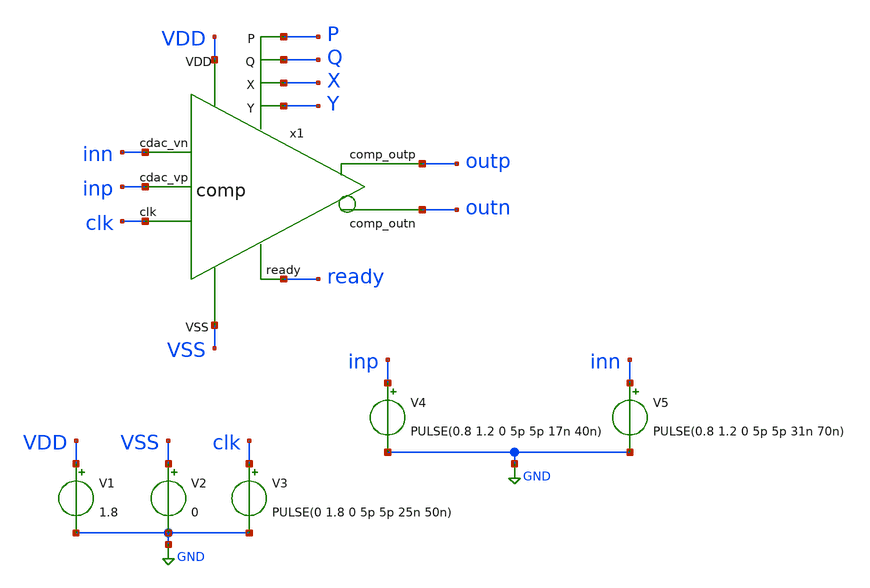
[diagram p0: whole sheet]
** sch_path: module/comparator/tb_comp.sch
**.subckt tb_comp
x1 X Y ready outn outp inn inp clk VDD VSS Q P comp
V1 VDD GND 1.8
V2 VSS GND 0
V3 clk GND PULSE(0 1.8 0 5p 5p 25n 50n)
V4 inp GND PULSE(0.8 1.2 0 5p 5p 17n 40n)
V5 inn GND PULSE(0.8 1.2 0 5p 5p 31n 70n)
**** begin user architecture code



.lib /foss/pdks/sky130A/libs.tech/ngspice/sky130.lib.spice tt

.tran 49ns 51ns
.control
    run
    plot V(outp)+8 V(P)-2  V(X)+4  V(clk) V(inn) V(inp) V(Y)+2  V(outn)+6 V(Q)-2 V(ready)+10
.endc
.save all



**** end user architecture code
**.ends

* expanding   symbol:  /foss/designs/goss_test/module/comparator/comp.sym # of pins=12
** sym_path: module/comparator/comp.sym
** sch_path: module/comparator/comp.sch
.subckt comp X Y ready comp_outn comp_outp cdac_vn cdac_vp clk VDD VSS Q P
*.ipin cdac_vn
*.ipin cdac_vp
*.ipin VSS
*.ipin VDD
*.opin comp_outp
*.opin comp_outn
*.opin ready
*.ipin clk
*.opin X
*.opin Y
*.opin P
*.opin Q
XM1 net1 clk VSS VSS sky130_fd_pr__nfet_01v8 L=0.15 W=4 nf=1 ad='int((nf+1)/2) * W/nf * 0.29' as='int((nf+2)/2) * W/nf * 0.29'
+ pd='2*int((nf+1)/2) * (W/nf + 0.29)' ps='2*int((nf+2)/2) * (W/nf + 0.29)' nrd='0.29 / W' nrs='0.29 / W'
+ sa=0 sb=0 sd=0 mult=1 m=1
XM2 P cdac_vp net1 VSS sky130_fd_pr__nfet_01v8 L=0.15 W=4 nf=1 ad='int((nf+1)/2) * W/nf * 0.29' as='int((nf+2)/2) * W/nf * 0.29'
+ pd='2*int((nf+1)/2) * (W/nf + 0.29)' ps='2*int((nf+2)/2) * (W/nf + 0.29)' nrd='0.29 / W' nrs='0.29 / W'
+ sa=0 sb=0 sd=0 mult=1 m=1
XM3 Q cdac_vn net1 VSS sky130_fd_pr__nfet_01v8 L=0.15 W=4 nf=1 ad='int((nf+1)/2) * W/nf * 0.29' as='int((nf+2)/2) * W/nf * 0.29'
+ pd='2*int((nf+1)/2) * (W/nf + 0.29)' ps='2*int((nf+2)/2) * (W/nf + 0.29)' nrd='0.29 / W' nrs='0.29 / W'
+ sa=0 sb=0 sd=0 mult=1 m=1
XM4 Y X Q VSS sky130_fd_pr__nfet_01v8 L=0.15 W=8 nf=1 ad='int((nf+1)/2) * W/nf * 0.29' as='int((nf+2)/2) * W/nf * 0.29'
+ pd='2*int((nf+1)/2) * (W/nf + 0.29)' ps='2*int((nf+2)/2) * (W/nf + 0.29)' nrd='0.29 / W' nrs='0.29 / W'
+ sa=0 sb=0 sd=0 mult=1 m=1
XM5 X Y P VSS sky130_fd_pr__nfet_01v8 L=0.15 W=8 nf=1 ad='int((nf+1)/2) * W/nf * 0.29' as='int((nf+2)/2) * W/nf * 0.29'
+ pd='2*int((nf+1)/2) * (W/nf + 0.29)' ps='2*int((nf+2)/2) * (W/nf + 0.29)' nrd='0.29 / W' nrs='0.29 / W'
+ sa=0 sb=0 sd=0 mult=1 m=1
XM6 X Y VDD VDD sky130_fd_pr__pfet_01v8 L=0.15 W=2 nf=1 ad='int((nf+1)/2) * W/nf * 0.29' as='int((nf+2)/2) * W/nf * 0.29'
+ pd='2*int((nf+1)/2) * (W/nf + 0.29)' ps='2*int((nf+2)/2) * (W/nf + 0.29)' nrd='0.29 / W' nrs='0.29 / W'
+ sa=0 sb=0 sd=0 mult=1 m=1
XM7 Y X VDD VDD sky130_fd_pr__pfet_01v8 L=0.15 W=2 nf=1 ad='int((nf+1)/2) * W/nf * 0.29' as='int((nf+2)/2) * W/nf * 0.29'
+ pd='2*int((nf+1)/2) * (W/nf + 0.29)' ps='2*int((nf+2)/2) * (W/nf + 0.29)' nrd='0.29 / W' nrs='0.29 / W'
+ sa=0 sb=0 sd=0 mult=1 m=1
XM8 X clk VDD VDD sky130_fd_pr__pfet_01v8 L=0.15 W=2 nf=1 ad='int((nf+1)/2) * W/nf * 0.29' as='int((nf+2)/2) * W/nf * 0.29'
+ pd='2*int((nf+1)/2) * (W/nf + 0.29)' ps='2*int((nf+2)/2) * (W/nf + 0.29)' nrd='0.29 / W' nrs='0.29 / W'
+ sa=0 sb=0 sd=0 mult=1 m=1
XM9 P clk VDD VDD sky130_fd_pr__pfet_01v8 L=0.15 W=2 nf=1 ad='int((nf+1)/2) * W/nf * 0.29' as='int((nf+2)/2) * W/nf * 0.29'
+ pd='2*int((nf+1)/2) * (W/nf + 0.29)' ps='2*int((nf+2)/2) * (W/nf + 0.29)' nrd='0.29 / W' nrs='0.29 / W'
+ sa=0 sb=0 sd=0 mult=1 m=1
XM10 Y clk VDD VDD sky130_fd_pr__pfet_01v8 L=0.15 W=2 nf=1 ad='int((nf+1)/2) * W/nf * 0.29' as='int((nf+2)/2) * W/nf * 0.29'
+ pd='2*int((nf+1)/2) * (W/nf + 0.29)' ps='2*int((nf+2)/2) * (W/nf + 0.29)' nrd='0.29 / W' nrs='0.29 / W'
+ sa=0 sb=0 sd=0 mult=1 m=1
XM11 Q clk VDD VDD sky130_fd_pr__pfet_01v8 L=0.15 W=2 nf=1 ad='int((nf+1)/2) * W/nf * 0.29' as='int((nf+2)/2) * W/nf * 0.29'
+ pd='2*int((nf+1)/2) * (W/nf + 0.29)' ps='2*int((nf+2)/2) * (W/nf + 0.29)' nrd='0.29 / W' nrs='0.29 / W'
+ sa=0 sb=0 sd=0 mult=1 m=1
XM12 X_inv X VDD VDD sky130_fd_pr__pfet_01v8 L=0.15 W=0.84 nf=1 ad='int((nf+1)/2) * W/nf * 0.29' as='int((nf+2)/2) * W/nf * 0.29'
+ pd='2*int((nf+1)/2) * (W/nf + 0.29)' ps='2*int((nf+2)/2) * (W/nf + 0.29)' nrd='0.29 / W' nrs='0.29 / W'
+ sa=0 sb=0 sd=0 mult=1 m=1
XM13 X_inv X VSS VSS sky130_fd_pr__nfet_01v8 L=0.15 W=0.42 nf=1 ad='int((nf+1)/2) * W/nf * 0.29' as='int((nf+2)/2) * W/nf * 0.29'
+ pd='2*int((nf+1)/2) * (W/nf + 0.29)' ps='2*int((nf+2)/2) * (W/nf + 0.29)' nrd='0.29 / W' nrs='0.29 / W'
+ sa=0 sb=0 sd=0 mult=1 m=1
XM14 Y_inv Y VDD VDD sky130_fd_pr__pfet_01v8 L=0.15 W=0.84 nf=1 ad='int((nf+1)/2) * W/nf * 0.29' as='int((nf+2)/2) * W/nf * 0.29'
+ pd='2*int((nf+1)/2) * (W/nf + 0.29)' ps='2*int((nf+2)/2) * (W/nf + 0.29)' nrd='0.29 / W' nrs='0.29 / W'
+ sa=0 sb=0 sd=0 mult=1 m=1
XM15 Y_inv Y VSS VSS sky130_fd_pr__nfet_01v8 L=0.15 W=0.42 nf=1 ad='int((nf+1)/2) * W/nf * 0.29' as='int((nf+2)/2) * W/nf * 0.29'
+ pd='2*int((nf+1)/2) * (W/nf + 0.29)' ps='2*int((nf+2)/2) * (W/nf + 0.29)' nrd='0.29 / W' nrs='0.29 / W'
+ sa=0 sb=0 sd=0 mult=1 m=1
XM16 comp_outp comp_outn VDD VDD sky130_fd_pr__pfet_01v8 L=0.15 W=0.84 nf=1 ad='int((nf+1)/2) * W/nf * 0.29'
+ as='int((nf+2)/2) * W/nf * 0.29' pd='2*int((nf+1)/2) * (W/nf + 0.29)' ps='2*int((nf+2)/2) * (W/nf + 0.29)'
+ nrd='0.29 / W' nrs='0.29 / W' sa=0 sb=0 sd=0 mult=1 m=1
XM17 comp_outn comp_outp VDD VDD sky130_fd_pr__pfet_01v8 L=0.15 W=0.84 nf=1 ad='int((nf+1)/2) * W/nf * 0.29'
+ as='int((nf+2)/2) * W/nf * 0.29' pd='2*int((nf+1)/2) * (W/nf + 0.29)' ps='2*int((nf+2)/2) * (W/nf + 0.29)'
+ nrd='0.29 / W' nrs='0.29 / W' sa=0 sb=0 sd=0 mult=1 m=1
XM18 ready Y net2 VSS sky130_fd_pr__nfet_01v8 L=0.15 W=0.42 nf=1 ad='int((nf+1)/2) * W/nf * 0.29' as='int((nf+2)/2) * W/nf * 0.29'
+ pd='2*int((nf+1)/2) * (W/nf + 0.29)' ps='2*int((nf+2)/2) * (W/nf + 0.29)' nrd='0.29 / W' nrs='0.29 / W'
+ sa=0 sb=0 sd=0 mult=1 m=1
XM19 comp_outn Y_inv VSS VSS sky130_fd_pr__nfet_01v8 L=0.15 W=4 nf=1 ad='int((nf+1)/2) * W/nf * 0.29'
+ as='int((nf+2)/2) * W/nf * 0.29' pd='2*int((nf+1)/2) * (W/nf + 0.29)' ps='2*int((nf+2)/2) * (W/nf + 0.29)'
+ nrd='0.29 / W' nrs='0.29 / W' sa=0 sb=0 sd=0 mult=1 m=1
XM20 ready Y X VDD sky130_fd_pr__pfet_01v8 L=0.15 W=0.84 nf=1 ad='int((nf+1)/2) * W/nf * 0.29' as='int((nf+2)/2) * W/nf * 0.29'
+ pd='2*int((nf+1)/2) * (W/nf + 0.29)' ps='2*int((nf+2)/2) * (W/nf + 0.29)' nrd='0.29 / W' nrs='0.29 / W'
+ sa=0 sb=0 sd=0 mult=1 m=1
XM21 ready X Y VDD sky130_fd_pr__pfet_01v8 L=0.15 W=0.84 nf=1 ad='int((nf+1)/2) * W/nf * 0.29' as='int((nf+2)/2) * W/nf * 0.29'
+ pd='2*int((nf+1)/2) * (W/nf + 0.29)' ps='2*int((nf+2)/2) * (W/nf + 0.29)' nrd='0.29 / W' nrs='0.29 / W'
+ sa=0 sb=0 sd=0 mult=1 m=1
XM22 net2 X VSS VSS sky130_fd_pr__nfet_01v8 L=0.15 W=4 nf=1 ad='int((nf+1)/2) * W/nf * 0.29' as='int((nf+2)/2) * W/nf * 0.29'
+ pd='2*int((nf+1)/2) * (W/nf + 0.29)' ps='2*int((nf+2)/2) * (W/nf + 0.29)' nrd='0.29 / W' nrs='0.29 / W'
+ sa=0 sb=0 sd=0 mult=1 m=1
XM23 comp_outp X_inv VSS VSS sky130_fd_pr__nfet_01v8 L=0.15 W=0.42 nf=1 ad='int((nf+1)/2) * W/nf * 0.29'
+ as='int((nf+2)/2) * W/nf * 0.29' pd='2*int((nf+1)/2) * (W/nf + 0.29)' ps='2*int((nf+2)/2) * (W/nf + 0.29)'
+ nrd='0.29 / W' nrs='0.29 / W' sa=0 sb=0 sd=0 mult=1 m=1
.ends

.GLOBAL GND
.end
